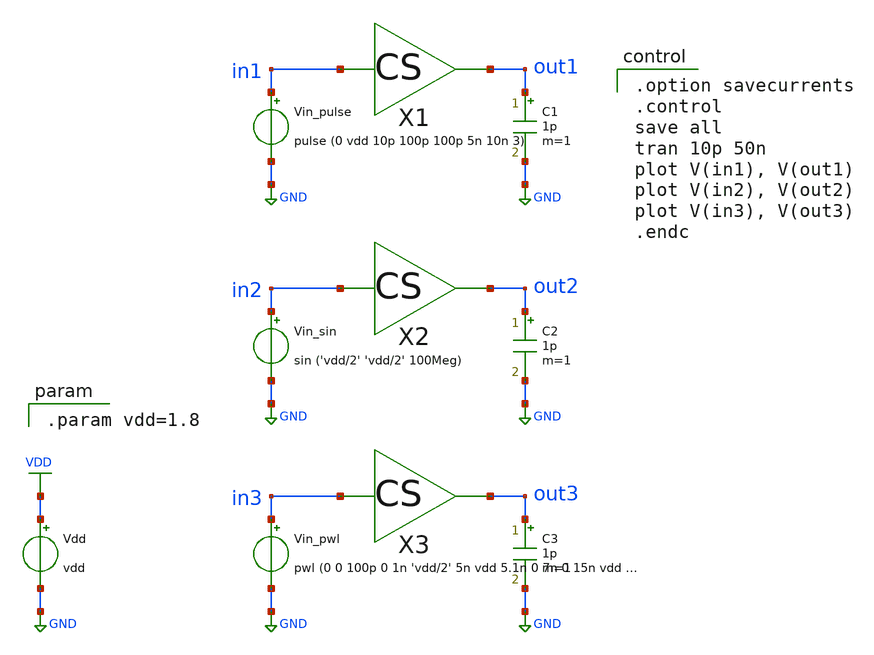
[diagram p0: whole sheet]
** sch_path: xschem/tb/tran_01.sch
**.subckt tran_01
Vdd VDD GND vdd
Vin_pulse in1 GND pulse (0 vdd 10p 100p 100p 5n 10n 3)
X1 in1 out1 cs
C1 out1 GND 1p m=1
Vin_sin in2 GND sin ('vdd/2' 'vdd/2' 100Meg)
X2 in2 out2 cs
C2 out2 GND 1p m=1
Vin_pwl in3 GND pwl (0 0 100p 0 1n 'vdd/2' 5n vdd 5.1n 0 7n 0 15n vdd 30n 'vdd/3' 40n 0 )
X3 in3 out3 cs
C3 out3 GND 1p m=1
**** begin user architecture code

.model nch nmos ( version=4.7 level=54 lmin=0.1u lmax=20u wmin=0.1u wmax=10u  )
.model pch pmos ( version=4.7 level=54 lmin=0.1u lmax=20u wmin=0.1u wmax=10u  )


.option savecurrents
.control
save all
tran 10p 50n
plot V(in1), V(out1)
plot V(in2), V(out2)
plot V(in3), V(out3)
.endc


.param vdd=1.8

**** end user architecture code
**.ends

* expanding   symbol:  cs.sym # of pins=2
** sym_path: xschem/tb/cs.sym
** sch_path: xschem/tb/cs.sch
.subckt cs in out
*.ipin in
*.opin out
R1 VDD out 1k m=1
M1 out in GND GND nch w=3.6u l=0.18u m=1
.ends

.GLOBAL VDD
.GLOBAL GND
.end
